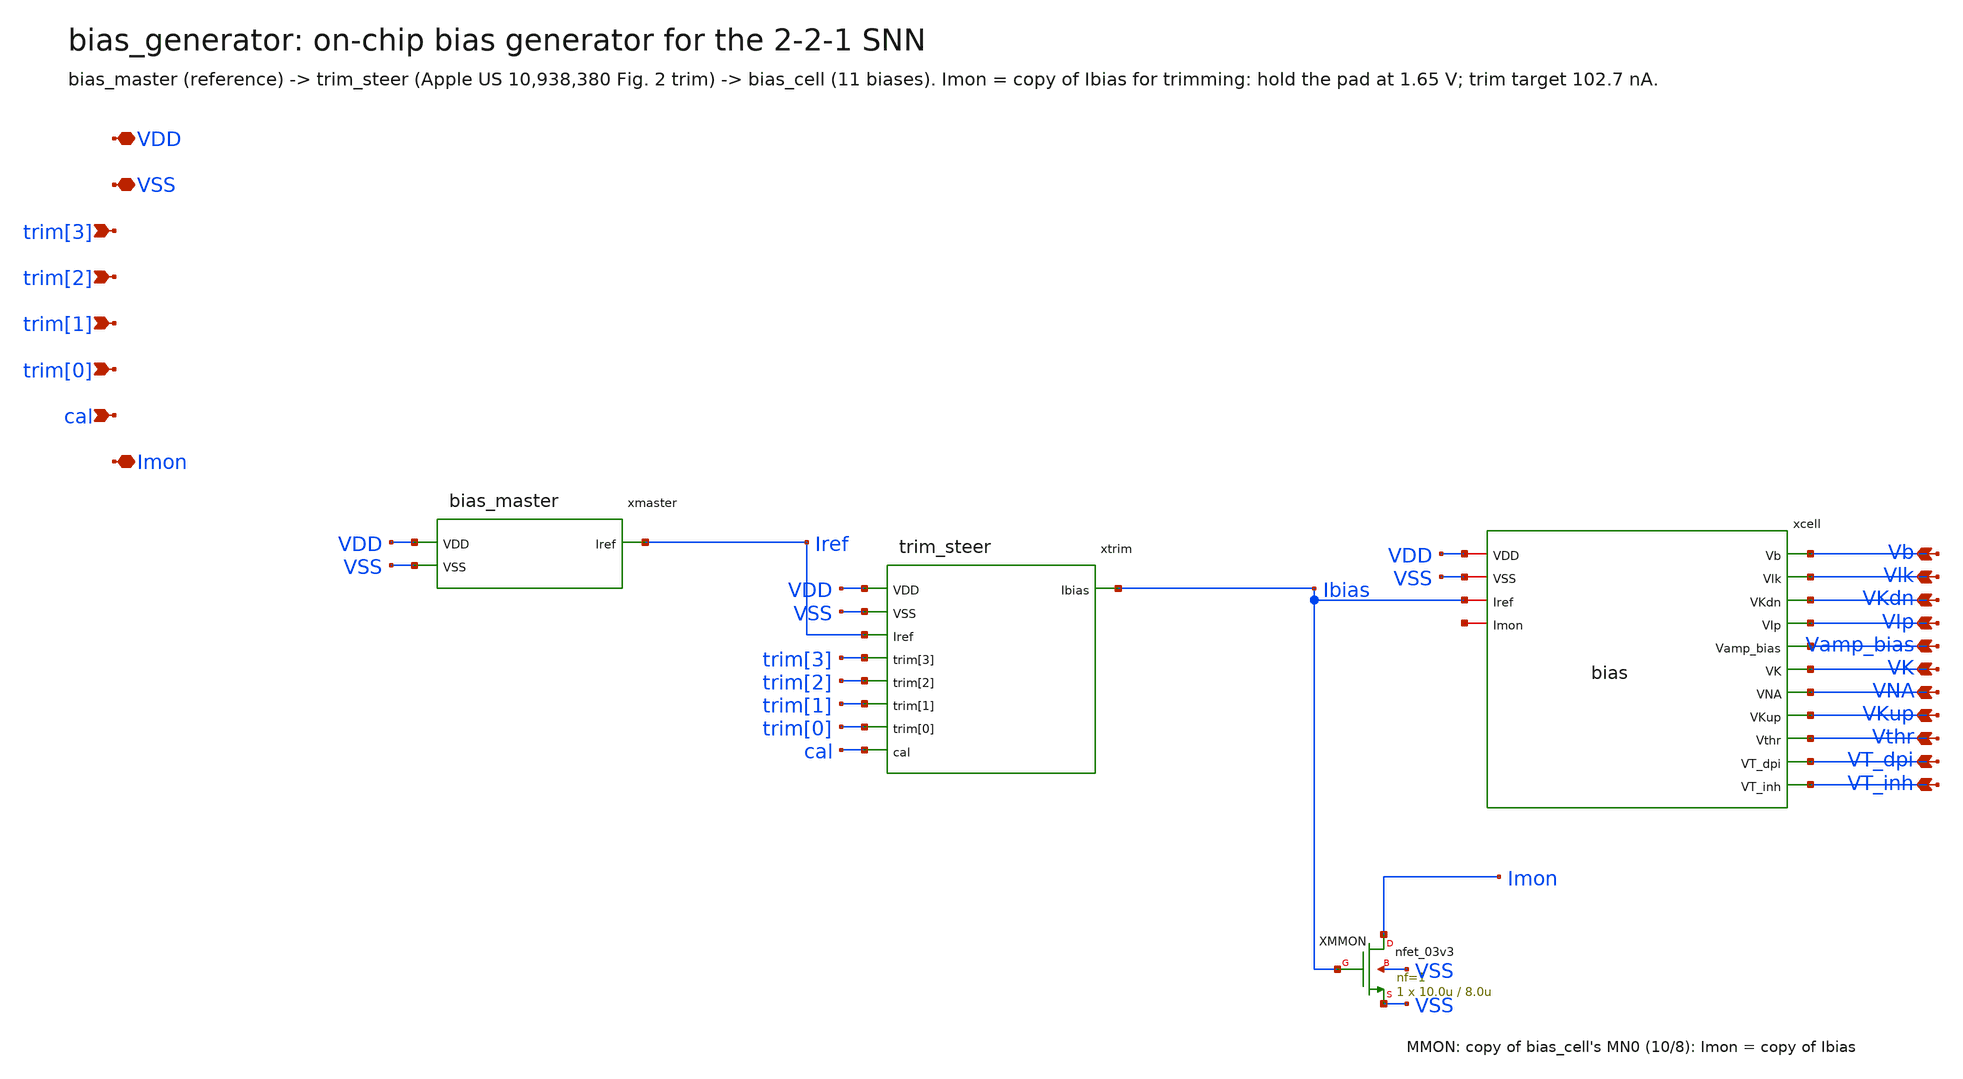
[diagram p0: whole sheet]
** sch_path: explore/bias/generator/bias_generator.sch
**.subckt bias_generator VDD VSS trim[3] trim[2] trim[1] trim[0] cal Imon Vb Vlk VKdn VIp Vamp_bias
*+ VK VNA VKup Vthr VT_dpi VT_inh
*.iopin VDD
*.iopin VSS
*.ipin trim[3]
*.ipin trim[2]
*.ipin trim[1]
*.ipin trim[0]
*.ipin cal
*.iopin Imon
*.opin Vb
*.opin Vlk
*.opin VKdn
*.opin VIp
*.opin Vamp_bias
*.opin VK
*.opin VNA
*.opin VKup
*.opin Vthr
*.opin VT_dpi
*.opin VT_inh
xmaster VDD VSS Iref bias_master
xtrim VDD VSS Iref Ibias trim[3] trim[2] trim[1] trim[0] cal trim_steer
xcell VDD VSS Ibias Vb Vlk VKdn VIp Vamp_bias VK VNA VKup Vthr VT_dpi VT_inh net1 bias
XMMON Imon Ibias VSS VSS nfet_03v3 L=8.0u W=10.0u nf=1 ad='int((nf+1)/2) * W/nf * 0.18u' as='int((nf+2)/2) * W/nf * 0.18u'
+ pd='2*int((nf+1)/2) * (W/nf + 0.18u)' ps='2*int((nf+2)/2) * (W/nf + 0.18u)' nrd='0.18u / W' nrs='0.18u / W'
+ sa=0 sb=0 sd=0 m=1
**.ends

* expanding   symbol:  explore/bias/generator/bias_master.sym # of pins=3
** sym_path: analog/bias/generator/bias_master.sym
** sch_path: analog/bias/generator/bias_master.sch
.subckt bias_master VDD VSS Iref
*.iopin VDD
*.iopin VSS
*.iopin Iref
XM3 Vgp Vgp VDD VDD pfet_03v3 L=6.0u W=1.0u nf=1 ad='int((nf+1)/2) * W/nf * 0.18u' as='int((nf+2)/2) * W/nf * 0.18u'
+ pd='2*int((nf+1)/2) * (W/nf + 0.18u)' ps='2*int((nf+2)/2) * (W/nf + 0.18u)' nrd='0.18u / W' nrs='0.18u / W'
+ sa=0 sb=0 sd=0 m=4
XM4 Vgn Vgp VDD VDD pfet_03v3 L=6.0u W=1.0u nf=1 ad='int((nf+1)/2) * W/nf * 0.18u' as='int((nf+2)/2) * W/nf * 0.18u'
+ pd='2*int((nf+1)/2) * (W/nf + 0.18u)' ps='2*int((nf+2)/2) * (W/nf + 0.18u)' nrd='0.18u / W' nrs='0.18u / W'
+ sa=0 sb=0 sd=0 m=4
XM2 Vgp Vgn Vr VSS nfet_03v3 L=6.0u W=1.0u nf=1 ad='int((nf+1)/2) * W/nf * 0.18u' as='int((nf+2)/2) * W/nf * 0.18u'
+ pd='2*int((nf+1)/2) * (W/nf + 0.18u)' ps='2*int((nf+2)/2) * (W/nf + 0.18u)' nrd='0.18u / W' nrs='0.18u / W'
+ sa=0 sb=0 sd=0 m=64
XM1 Vgn Vgn VSS VSS nfet_03v3 L=6.0u W=1.0u nf=1 ad='int((nf+1)/2) * W/nf * 0.18u' as='int((nf+2)/2) * W/nf * 0.18u'
+ pd='2*int((nf+1)/2) * (W/nf + 0.18u)' ps='2*int((nf+2)/2) * (W/nf + 0.18u)' nrd='0.18u / W' nrs='0.18u / W'
+ sa=0 sb=0 sd=0 m=8
XR VSS Vr VSS nwell r_width=2.0e-6 r_length=585.380e-6 m=1
XMS1_0 net1 VSS VDD VDD pfet_03v3 L=45.45u W=0.5u nf=1 ad='int((nf+1)/2) * W/nf * 0.18u' as='int((nf+2)/2) * W/nf * 0.18u'
+ pd='2*int((nf+1)/2) * (W/nf + 0.18u)' ps='2*int((nf+2)/2) * (W/nf + 0.18u)' nrd='0.18u / W' nrs='0.18u / W'
+ sa=0 sb=0 sd=0 m=1
XMS1_1 net2 VSS net1 VDD pfet_03v3 L=45.45u W=0.5u nf=1 ad='int((nf+1)/2) * W/nf * 0.18u' as='int((nf+2)/2) * W/nf * 0.18u'
+ pd='2*int((nf+1)/2) * (W/nf + 0.18u)' ps='2*int((nf+2)/2) * (W/nf + 0.18u)' nrd='0.18u / W' nrs='0.18u / W'
+ sa=0 sb=0 sd=0 m=1
XMS1_2 net3 VSS net2 VDD pfet_03v3 L=45.45u W=0.5u nf=1 ad='int((nf+1)/2) * W/nf * 0.18u' as='int((nf+2)/2) * W/nf * 0.18u'
+ pd='2*int((nf+1)/2) * (W/nf + 0.18u)' ps='2*int((nf+2)/2) * (W/nf + 0.18u)' nrd='0.18u / W' nrs='0.18u / W'
+ sa=0 sb=0 sd=0 m=1
XMS1_3 s4 VSS net3 VDD pfet_03v3 L=45.45u W=0.5u nf=1 ad='int((nf+1)/2) * W/nf * 0.18u' as='int((nf+2)/2) * W/nf * 0.18u'
+ pd='2*int((nf+1)/2) * (W/nf + 0.18u)' ps='2*int((nf+2)/2) * (W/nf + 0.18u)' nrd='0.18u / W' nrs='0.18u / W'
+ sa=0 sb=0 sd=0 m=1
XMS2 X Vgn VSS VSS nfet_03v3 L=6.0u W=1.0u nf=1 ad='int((nf+1)/2) * W/nf * 0.18u' as='int((nf+2)/2) * W/nf * 0.18u'
+ pd='2*int((nf+1)/2) * (W/nf + 0.18u)' ps='2*int((nf+2)/2) * (W/nf + 0.18u)' nrd='0.18u / W' nrs='0.18u / W'
+ sa=0 sb=0 sd=0 m=16
XMS3 Vgp X VSS VSS nfet_03v3 L=4u W=0.5u nf=1 ad='int((nf+1)/2) * W/nf * 0.18u' as='int((nf+2)/2) * W/nf * 0.18u'
+ pd='2*int((nf+1)/2) * (W/nf + 0.18u)' ps='2*int((nf+2)/2) * (W/nf + 0.18u)' nrd='0.18u / W' nrs='0.18u / W'
+ sa=0 sb=0 sd=0 m=1
XMREF Iref Vgn VSS VSS nfet_03v3 L=6.0u W=1.0u nf=1 ad='int((nf+1)/2) * W/nf * 0.18u' as='int((nf+2)/2) * W/nf * 0.18u'
+ pd='2*int((nf+1)/2) * (W/nf + 0.18u)' ps='2*int((nf+2)/2) * (W/nf + 0.18u)' nrd='0.18u / W' nrs='0.18u / W'
+ sa=0 sb=0 sd=0 m=4
XMS1_4 net4 VSS s4 VDD pfet_03v3 L=45.45u W=0.5u nf=1 ad='int((nf+1)/2) * W/nf * 0.18u' as='int((nf+2)/2) * W/nf * 0.18u'
+ pd='2*int((nf+1)/2) * (W/nf + 0.18u)' ps='2*int((nf+2)/2) * (W/nf + 0.18u)' nrd='0.18u / W' nrs='0.18u / W'
+ sa=0 sb=0 sd=0 m=1
XMS1_5 net5 VSS net4 VDD pfet_03v3 L=45.45u W=0.5u nf=1 ad='int((nf+1)/2) * W/nf * 0.18u' as='int((nf+2)/2) * W/nf * 0.18u'
+ pd='2*int((nf+1)/2) * (W/nf + 0.18u)' ps='2*int((nf+2)/2) * (W/nf + 0.18u)' nrd='0.18u / W' nrs='0.18u / W'
+ sa=0 sb=0 sd=0 m=1
XMS1_6 net6 VSS net5 VDD pfet_03v3 L=45.45u W=0.5u nf=1 ad='int((nf+1)/2) * W/nf * 0.18u' as='int((nf+2)/2) * W/nf * 0.18u'
+ pd='2*int((nf+1)/2) * (W/nf + 0.18u)' ps='2*int((nf+2)/2) * (W/nf + 0.18u)' nrd='0.18u / W' nrs='0.18u / W'
+ sa=0 sb=0 sd=0 m=1
XMS1_7 net7 VSS net6 VDD pfet_03v3 L=45.45u W=0.5u nf=1 ad='int((nf+1)/2) * W/nf * 0.18u' as='int((nf+2)/2) * W/nf * 0.18u'
+ pd='2*int((nf+1)/2) * (W/nf + 0.18u)' ps='2*int((nf+2)/2) * (W/nf + 0.18u)' nrd='0.18u / W' nrs='0.18u / W'
+ sa=0 sb=0 sd=0 m=1
XMS1_8 net8 VSS net7 VDD pfet_03v3 L=45.45u W=0.5u nf=1 ad='int((nf+1)/2) * W/nf * 0.18u' as='int((nf+2)/2) * W/nf * 0.18u'
+ pd='2*int((nf+1)/2) * (W/nf + 0.18u)' ps='2*int((nf+2)/2) * (W/nf + 0.18u)' nrd='0.18u / W' nrs='0.18u / W'
+ sa=0 sb=0 sd=0 m=1
XMS1_9 X VSS net8 VDD pfet_03v3 L=45.45u W=0.5u nf=1 ad='int((nf+1)/2) * W/nf * 0.18u' as='int((nf+2)/2) * W/nf * 0.18u'
+ pd='2*int((nf+1)/2) * (W/nf + 0.18u)' ps='2*int((nf+2)/2) * (W/nf + 0.18u)' nrd='0.18u / W' nrs='0.18u / W'
+ sa=0 sb=0 sd=0 m=1
.ends


* expanding   symbol:  explore/bias/generator/trim_steer.sym # of pins=9
** sym_path: analog/bias/generator/trim_steer.sym
** sch_path: analog/bias/generator/trim_steer.sch
.subckt trim_steer VDD VSS Iref Ibias trim[3] trim[2] trim[1] trim[0] cal
*.iopin VDD
*.iopin VSS
*.iopin Iref
*.ipin trim[3]
*.ipin trim[2]
*.ipin trim[1]
*.ipin trim[0]
*.ipin cal
*.opin Ibias
XM0 Iref Iref VDD VDD pfet_03v3 L=6.0u W=1.0u nf=1 ad='int((nf+1)/2) * W/nf * 0.18u' as='int((nf+2)/2) * W/nf * 0.18u'
+ pd='2*int((nf+1)/2) * (W/nf + 0.18u)' ps='2*int((nf+2)/2) * (W/nf + 0.18u)' nrd='0.18u / W' nrs='0.18u / W'
+ sa=0 sb=0 sd=0 m=23
XR0 Iref Vgs VSS nwell r_width=2.0e-6 r_length=150.000e-6 m=1
XMCG VDD Vgs VDD VDD pfet_03v3 L=10.0u W=10.0u nf=1 ad='int((nf+1)/2) * W/nf * 0.18u' as='int((nf+2)/2) * W/nf * 0.18u'
+ pd='2*int((nf+1)/2) * (W/nf + 0.18u)' ps='2*int((nf+2)/2) * (W/nf + 0.18u)' nrd='0.18u / W' nrs='0.18u / W'
+ sa=0 sb=0 sd=0 m=1
XMB net1 Vgs VDD VDD pfet_03v3 L=6.0u W=1.0u nf=1 ad='int((nf+1)/2) * W/nf * 0.18u' as='int((nf+2)/2) * W/nf * 0.18u'
+ pd='2*int((nf+1)/2) * (W/nf + 0.18u)' ps='2*int((nf+2)/2) * (W/nf + 0.18u)' nrd='0.18u / W' nrs='0.18u / W'
+ sa=0 sb=0 sd=0 m=14
XSB net1 VDD Ibias VSS nfet_03v3 L=0.5u W=1.0u nf=1 ad='int((nf+1)/2) * W/nf * 0.18u' as='int((nf+2)/2) * W/nf * 0.18u'
+ pd='2*int((nf+1)/2) * (W/nf + 0.18u)' ps='2*int((nf+2)/2) * (W/nf + 0.18u)' nrd='0.18u / W' nrs='0.18u / W'
+ sa=0 sb=0 sd=0 m=1
XM1 net2 Vgs VDD VDD pfet_03v3 L=6.0u W=1.0u nf=1 ad='int((nf+1)/2) * W/nf * 0.18u' as='int((nf+2)/2) * W/nf * 0.18u'
+ pd='2*int((nf+1)/2) * (W/nf + 0.18u)' ps='2*int((nf+2)/2) * (W/nf + 0.18u)' nrd='0.18u / W' nrs='0.18u / W'
+ sa=0 sb=0 sd=0 m=1
XS0 net2 trim[0] Ibias VSS nfet_03v3 L=0.5u W=1.0u nf=1 ad='int((nf+1)/2) * W/nf * 0.18u' as='int((nf+2)/2) * W/nf * 0.18u'
+ pd='2*int((nf+1)/2) * (W/nf + 0.18u)' ps='2*int((nf+2)/2) * (W/nf + 0.18u)' nrd='0.18u / W' nrs='0.18u / W'
+ sa=0 sb=0 sd=0 m=1
XS0X net2 tb0 aux VSS nfet_03v3 L=0.5u W=1.0u nf=1 ad='int((nf+1)/2) * W/nf * 0.18u' as='int((nf+2)/2) * W/nf * 0.18u'
+ pd='2*int((nf+1)/2) * (W/nf + 0.18u)' ps='2*int((nf+2)/2) * (W/nf + 0.18u)' nrd='0.18u / W' nrs='0.18u / W'
+ sa=0 sb=0 sd=0 m=1
XM2 net3 Vgs VDD VDD pfet_03v3 L=6.0u W=1.0u nf=1 ad='int((nf+1)/2) * W/nf * 0.18u' as='int((nf+2)/2) * W/nf * 0.18u'
+ pd='2*int((nf+1)/2) * (W/nf + 0.18u)' ps='2*int((nf+2)/2) * (W/nf + 0.18u)' nrd='0.18u / W' nrs='0.18u / W'
+ sa=0 sb=0 sd=0 m=2
XS1 net3 trim[1] Ibias VSS nfet_03v3 L=0.5u W=1.0u nf=1 ad='int((nf+1)/2) * W/nf * 0.18u' as='int((nf+2)/2) * W/nf * 0.18u'
+ pd='2*int((nf+1)/2) * (W/nf + 0.18u)' ps='2*int((nf+2)/2) * (W/nf + 0.18u)' nrd='0.18u / W' nrs='0.18u / W'
+ sa=0 sb=0 sd=0 m=1
XS1X net3 tb1 aux VSS nfet_03v3 L=0.5u W=1.0u nf=1 ad='int((nf+1)/2) * W/nf * 0.18u' as='int((nf+2)/2) * W/nf * 0.18u'
+ pd='2*int((nf+1)/2) * (W/nf + 0.18u)' ps='2*int((nf+2)/2) * (W/nf + 0.18u)' nrd='0.18u / W' nrs='0.18u / W'
+ sa=0 sb=0 sd=0 m=1
XM3 net4 Vgs VDD VDD pfet_03v3 L=6.0u W=1.0u nf=1 ad='int((nf+1)/2) * W/nf * 0.18u' as='int((nf+2)/2) * W/nf * 0.18u'
+ pd='2*int((nf+1)/2) * (W/nf + 0.18u)' ps='2*int((nf+2)/2) * (W/nf + 0.18u)' nrd='0.18u / W' nrs='0.18u / W'
+ sa=0 sb=0 sd=0 m=4
XS2 net4 trim[2] Ibias VSS nfet_03v3 L=0.5u W=1.0u nf=1 ad='int((nf+1)/2) * W/nf * 0.18u' as='int((nf+2)/2) * W/nf * 0.18u'
+ pd='2*int((nf+1)/2) * (W/nf + 0.18u)' ps='2*int((nf+2)/2) * (W/nf + 0.18u)' nrd='0.18u / W' nrs='0.18u / W'
+ sa=0 sb=0 sd=0 m=1
XS2X net4 tb2 aux VSS nfet_03v3 L=0.5u W=1.0u nf=1 ad='int((nf+1)/2) * W/nf * 0.18u' as='int((nf+2)/2) * W/nf * 0.18u'
+ pd='2*int((nf+1)/2) * (W/nf + 0.18u)' ps='2*int((nf+2)/2) * (W/nf + 0.18u)' nrd='0.18u / W' nrs='0.18u / W'
+ sa=0 sb=0 sd=0 m=1
XM4 net5 Vgs VDD VDD pfet_03v3 L=6.0u W=1.0u nf=1 ad='int((nf+1)/2) * W/nf * 0.18u' as='int((nf+2)/2) * W/nf * 0.18u'
+ pd='2*int((nf+1)/2) * (W/nf + 0.18u)' ps='2*int((nf+2)/2) * (W/nf + 0.18u)' nrd='0.18u / W' nrs='0.18u / W'
+ sa=0 sb=0 sd=0 m=8
XS3 net5 trim[3] Ibias VSS nfet_03v3 L=0.5u W=1.0u nf=1 ad='int((nf+1)/2) * W/nf * 0.18u' as='int((nf+2)/2) * W/nf * 0.18u'
+ pd='2*int((nf+1)/2) * (W/nf + 0.18u)' ps='2*int((nf+2)/2) * (W/nf + 0.18u)' nrd='0.18u / W' nrs='0.18u / W'
+ sa=0 sb=0 sd=0 m=1
XS3X net5 tb3 aux VSS nfet_03v3 L=0.5u W=1.0u nf=1 ad='int((nf+1)/2) * W/nf * 0.18u' as='int((nf+2)/2) * W/nf * 0.18u'
+ pd='2*int((nf+1)/2) * (W/nf + 0.18u)' ps='2*int((nf+2)/2) * (W/nf + 0.18u)' nrd='0.18u / W' nrs='0.18u / W'
+ sa=0 sb=0 sd=0 m=1
XMIP0 tb0 trim[0] VDD VDD pfet_03v3 L=0.28u W=1.0u nf=1 ad='int((nf+1)/2) * W/nf * 0.18u' as='int((nf+2)/2) * W/nf * 0.18u'
+ pd='2*int((nf+1)/2) * (W/nf + 0.18u)' ps='2*int((nf+2)/2) * (W/nf + 0.18u)' nrd='0.18u / W' nrs='0.18u / W'
+ sa=0 sb=0 sd=0 m=1
XMIN0 tb0 trim[0] VSS VSS nfet_03v3 L=0.28u W=0.5u nf=1 ad='int((nf+1)/2) * W/nf * 0.18u' as='int((nf+2)/2) * W/nf * 0.18u'
+ pd='2*int((nf+1)/2) * (W/nf + 0.18u)' ps='2*int((nf+2)/2) * (W/nf + 0.18u)' nrd='0.18u / W' nrs='0.18u / W'
+ sa=0 sb=0 sd=0 m=1
XMIP1 tb1 trim[1] VDD VDD pfet_03v3 L=0.28u W=1.0u nf=1 ad='int((nf+1)/2) * W/nf * 0.18u' as='int((nf+2)/2) * W/nf * 0.18u'
+ pd='2*int((nf+1)/2) * (W/nf + 0.18u)' ps='2*int((nf+2)/2) * (W/nf + 0.18u)' nrd='0.18u / W' nrs='0.18u / W'
+ sa=0 sb=0 sd=0 m=1
XMIN1 tb1 trim[1] VSS VSS nfet_03v3 L=0.28u W=0.5u nf=1 ad='int((nf+1)/2) * W/nf * 0.18u' as='int((nf+2)/2) * W/nf * 0.18u'
+ pd='2*int((nf+1)/2) * (W/nf + 0.18u)' ps='2*int((nf+2)/2) * (W/nf + 0.18u)' nrd='0.18u / W' nrs='0.18u / W'
+ sa=0 sb=0 sd=0 m=1
XMIP2 tb2 trim[2] VDD VDD pfet_03v3 L=0.28u W=1.0u nf=1 ad='int((nf+1)/2) * W/nf * 0.18u' as='int((nf+2)/2) * W/nf * 0.18u'
+ pd='2*int((nf+1)/2) * (W/nf + 0.18u)' ps='2*int((nf+2)/2) * (W/nf + 0.18u)' nrd='0.18u / W' nrs='0.18u / W'
+ sa=0 sb=0 sd=0 m=1
XMIN2 tb2 trim[2] VSS VSS nfet_03v3 L=0.28u W=0.5u nf=1 ad='int((nf+1)/2) * W/nf * 0.18u' as='int((nf+2)/2) * W/nf * 0.18u'
+ pd='2*int((nf+1)/2) * (W/nf + 0.18u)' ps='2*int((nf+2)/2) * (W/nf + 0.18u)' nrd='0.18u / W' nrs='0.18u / W'
+ sa=0 sb=0 sd=0 m=1
XMIP3 tb3 trim[3] VDD VDD pfet_03v3 L=0.28u W=1.0u nf=1 ad='int((nf+1)/2) * W/nf * 0.18u' as='int((nf+2)/2) * W/nf * 0.18u'
+ pd='2*int((nf+1)/2) * (W/nf + 0.18u)' ps='2*int((nf+2)/2) * (W/nf + 0.18u)' nrd='0.18u / W' nrs='0.18u / W'
+ sa=0 sb=0 sd=0 m=1
XMIN3 tb3 trim[3] VSS VSS nfet_03v3 L=0.28u W=0.5u nf=1 ad='int((nf+1)/2) * W/nf * 0.18u' as='int((nf+2)/2) * W/nf * 0.18u'
+ pd='2*int((nf+1)/2) * (W/nf + 0.18u)' ps='2*int((nf+2)/2) * (W/nf + 0.18u)' nrd='0.18u / W' nrs='0.18u / W'
+ sa=0 sb=0 sd=0 m=1
XMAUX aux vaux VSS VSS nfet_03v3 L=8.0u W=10.0u nf=1 ad='int((nf+1)/2) * W/nf * 0.18u' as='int((nf+2)/2) * W/nf * 0.18u'
+ pd='2*int((nf+1)/2) * (W/nf + 0.18u)' ps='2*int((nf+2)/2) * (W/nf + 0.18u)' nrd='0.18u / W' nrs='0.18u / W'
+ sa=0 sb=0 sd=0 m=1
XMCAL aux cal vaux VSS nfet_03v3 L=0.5u W=1.0u nf=1 ad='int((nf+1)/2) * W/nf * 0.18u' as='int((nf+2)/2) * W/nf * 0.18u'
+ pd='2*int((nf+1)/2) * (W/nf + 0.18u)' ps='2*int((nf+2)/2) * (W/nf + 0.18u)' nrd='0.18u / W' nrs='0.18u / W'
+ sa=0 sb=0 sd=0 m=1
XMDIS vaux calb VSS VSS nfet_03v3 L=45.45u W=0.5u nf=1 ad='int((nf+1)/2) * W/nf * 0.18u' as='int((nf+2)/2) * W/nf * 0.18u'
+ pd='2*int((nf+1)/2) * (W/nf + 0.18u)' ps='2*int((nf+2)/2) * (W/nf + 0.18u)' nrd='0.18u / W' nrs='0.18u / W'
+ sa=0 sb=0 sd=0 m=1
XMCAUX VSS vaux VSS VSS nfet_03v3 L=5.0u W=5.0u nf=1 ad='int((nf+1)/2) * W/nf * 0.18u' as='int((nf+2)/2) * W/nf * 0.18u'
+ pd='2*int((nf+1)/2) * (W/nf + 0.18u)' ps='2*int((nf+2)/2) * (W/nf + 0.18u)' nrd='0.18u / W' nrs='0.18u / W'
+ sa=0 sb=0 sd=0 m=1
XMIPC calb cal VDD VDD pfet_03v3 L=0.28u W=1.0u nf=1 ad='int((nf+1)/2) * W/nf * 0.18u' as='int((nf+2)/2) * W/nf * 0.18u'
+ pd='2*int((nf+1)/2) * (W/nf + 0.18u)' ps='2*int((nf+2)/2) * (W/nf + 0.18u)' nrd='0.18u / W' nrs='0.18u / W'
+ sa=0 sb=0 sd=0 m=1
XMINC calb cal VSS VSS nfet_03v3 L=0.28u W=0.5u nf=1 ad='int((nf+1)/2) * W/nf * 0.18u' as='int((nf+2)/2) * W/nf * 0.18u'
+ pd='2*int((nf+1)/2) * (W/nf + 0.18u)' ps='2*int((nf+2)/2) * (W/nf + 0.18u)' nrd='0.18u / W' nrs='0.18u / W'
+ sa=0 sb=0 sd=0 m=1
.ends


* expanding   symbol:  bias.sym # of pins=15
** sym_path: analog/neuron/bias.sym
** sch_path: analog/neuron/bias.sch
.subckt bias VDD VSS Iref Vb Vlk VKdn VIp Vamp_bias VK VNA VKup Vthr VT_dpi VT_inh Imon
*.iopin VDD
*.iopin VSS
*.iopin Iref
*.opin Vb
*.opin Vlk
*.opin VKdn
*.opin VIp
*.opin Vamp_bias
*.opin VK
*.opin VNA
*.opin VKup
*.opin Vthr
*.opin VT_dpi
*.opin VT_inh
*.iopin Imon
XMN0 Iref Iref VSS VSS nfet_03v3 L=8u W=10u nf=1 ad='int((nf+1)/2) * W/nf * 0.18u' as='int((nf+2)/2) * W/nf * 0.18u'
+ pd='2*int((nf+1)/2) * (W/nf + 0.18u)' ps='2*int((nf+2)/2) * (W/nf + 0.18u)' nrd='0.18u / W' nrs='0.18u / W'
+ sa=0 sb=0 sd=0 m=1
XMNP vgp Iref VSS VSS nfet_03v3 L=8u W=10u nf=1 ad='int((nf+1)/2) * W/nf * 0.18u' as='int((nf+2)/2) * W/nf * 0.18u'
+ pd='2*int((nf+1)/2) * (W/nf + 0.18u)' ps='2*int((nf+2)/2) * (W/nf + 0.18u)' nrd='0.18u / W' nrs='0.18u / W'
+ sa=0 sb=0 sd=0 m=1
XMP0 vgp vgp VDD VDD pfet_03v3 L=8u W=10u nf=1 ad='int((nf+1)/2) * W/nf * 0.18u' as='int((nf+2)/2) * W/nf * 0.18u'
+ pd='2*int((nf+1)/2) * (W/nf + 0.18u)' ps='2*int((nf+2)/2) * (W/nf + 0.18u)' nrd='0.18u / W' nrs='0.18u / W'
+ sa=0 sb=0 sd=0 m=1
XMO_Vb Vb vgp VDD VDD pfet_03v3 L=8u W=1.44u nf=1 ad='int((nf+1)/2) * W/nf * 0.18u' as='int((nf+2)/2) * W/nf * 0.18u'
+ pd='2*int((nf+1)/2) * (W/nf + 0.18u)' ps='2*int((nf+2)/2) * (W/nf + 0.18u)' nrd='0.18u / W' nrs='0.18u / W'
+ sa=0 sb=0 sd=0 m=1
XMR_Vb Vb Vb VSS VSS nfet_03v3 L=8u W=1u nf=1 ad='int((nf+1)/2) * W/nf * 0.18u' as='int((nf+2)/2) * W/nf * 0.18u'
+ pd='2*int((nf+1)/2) * (W/nf + 0.18u)' ps='2*int((nf+2)/2) * (W/nf + 0.18u)' nrd='0.18u / W' nrs='0.18u / W'
+ sa=0 sb=0 sd=0 m=1
XMO_Vlk Vlk vgp VDD VDD pfet_03v3 L=16u W=0.84u nf=1 ad='int((nf+1)/2) * W/nf * 0.18u' as='int((nf+2)/2) * W/nf * 0.18u'
+ pd='2*int((nf+1)/2) * (W/nf + 0.18u)' ps='2*int((nf+2)/2) * (W/nf + 0.18u)' nrd='0.18u / W' nrs='0.18u / W'
+ sa=0 sb=0 sd=0 m=1
XMR_Vlk Vlk Vlk VSS VSS nfet_03v3 L=1u W=1u nf=1 ad='int((nf+1)/2) * W/nf * 0.18u' as='int((nf+2)/2) * W/nf * 0.18u'
+ pd='2*int((nf+1)/2) * (W/nf + 0.18u)' ps='2*int((nf+2)/2) * (W/nf + 0.18u)' nrd='0.18u / W' nrs='0.18u / W'
+ sa=0 sb=0 sd=0 m=8
XMO_VKdn VKdn vgp VDD VDD pfet_03v3 L=8u W=12.94u nf=1 ad='int((nf+1)/2) * W/nf * 0.18u' as='int((nf+2)/2) * W/nf * 0.18u'
+ pd='2*int((nf+1)/2) * (W/nf + 0.18u)' ps='2*int((nf+2)/2) * (W/nf + 0.18u)' nrd='0.18u / W' nrs='0.18u / W'
+ sa=0 sb=0 sd=0 m=1
XMR_VKdn VKdn VKdn VSS VSS nfet_03v3 L=1u W=1u nf=1 ad='int((nf+1)/2) * W/nf * 0.18u' as='int((nf+2)/2) * W/nf * 0.18u'
+ pd='2*int((nf+1)/2) * (W/nf + 0.18u)' ps='2*int((nf+2)/2) * (W/nf + 0.18u)' nrd='0.18u / W' nrs='0.18u / W'
+ sa=0 sb=0 sd=0 m=4
XMO_VIp VIp vgp VDD VDD pfet_03v3 L=8u W=2.34u nf=1 ad='int((nf+1)/2) * W/nf * 0.18u' as='int((nf+2)/2) * W/nf * 0.18u'
+ pd='2*int((nf+1)/2) * (W/nf + 0.18u)' ps='2*int((nf+2)/2) * (W/nf + 0.18u)' nrd='0.18u / W' nrs='0.18u / W'
+ sa=0 sb=0 sd=0 m=1
XMR_VIp VIp VIp VSS VSS nfet_03v3 L=1u W=1u nf=1 ad='int((nf+1)/2) * W/nf * 0.18u' as='int((nf+2)/2) * W/nf * 0.18u'
+ pd='2*int((nf+1)/2) * (W/nf + 0.18u)' ps='2*int((nf+2)/2) * (W/nf + 0.18u)' nrd='0.18u / W' nrs='0.18u / W'
+ sa=0 sb=0 sd=0 m=1
XMO_Vamp_bias Vamp_bias vgp VDD VDD pfet_03v3 L=8u W=9.14u nf=1 ad='int((nf+1)/2) * W/nf * 0.18u' as='int((nf+2)/2) * W/nf * 0.18u'
+ pd='2*int((nf+1)/2) * (W/nf + 0.18u)' ps='2*int((nf+2)/2) * (W/nf + 0.18u)' nrd='0.18u / W' nrs='0.18u / W'
+ sa=0 sb=0 sd=0 m=1
XMR_Vamp_bias Vamp_bias Vamp_bias VSS VSS nfet_03v3 L=0.64u W=0.5u nf=1 ad='int((nf+1)/2) * W/nf * 0.18u'
+ as='int((nf+2)/2) * W/nf * 0.18u' pd='2*int((nf+1)/2) * (W/nf + 0.18u)' ps='2*int((nf+2)/2) * (W/nf + 0.18u)'
+ nrd='0.18u / W' nrs='0.18u / W' sa=0 sb=0 sd=0 m=1
XMO_VK VK vgp VDD VDD pfet_03v3 L=8u W=10.45u nf=1 ad='int((nf+1)/2) * W/nf * 0.18u' as='int((nf+2)/2) * W/nf * 0.18u'
+ pd='2*int((nf+1)/2) * (W/nf + 0.18u)' ps='2*int((nf+2)/2) * (W/nf + 0.18u)' nrd='0.18u / W' nrs='0.18u / W'
+ sa=0 sb=0 sd=0 m=1
XMR_VK VK VK vk_mid VSS nfet_03v3 L=45.45u W=0.5u nf=1 ad='int((nf+1)/2) * W/nf * 0.18u' as='int((nf+2)/2) * W/nf * 0.18u'
+ pd='2*int((nf+1)/2) * (W/nf + 0.18u)' ps='2*int((nf+2)/2) * (W/nf + 0.18u)' nrd='0.18u / W' nrs='0.18u / W'
+ sa=0 sb=0 sd=0 m=1
XMR_VNA VNA VNA VDD VDD pfet_03v3 L=45.45u W=0.5u nf=1 ad='int((nf+1)/2) * W/nf * 0.18u' as='int((nf+2)/2) * W/nf * 0.18u'
+ pd='2*int((nf+1)/2) * (W/nf + 0.18u)' ps='2*int((nf+2)/2) * (W/nf + 0.18u)' nrd='0.18u / W' nrs='0.18u / W'
+ sa=0 sb=0 sd=0 m=1
XMO_VNA VNA Iref VSS VSS nfet_03v3 L=8u W=5.76u nf=1 ad='int((nf+1)/2) * W/nf * 0.18u' as='int((nf+2)/2) * W/nf * 0.18u'
+ pd='2*int((nf+1)/2) * (W/nf + 0.18u)' ps='2*int((nf+2)/2) * (W/nf + 0.18u)' nrd='0.18u / W' nrs='0.18u / W'
+ sa=0 sb=0 sd=0 m=1
XMR_VKup VKup VKup VDD VDD pfet_03v3 L=8u W=1u nf=1 ad='int((nf+1)/2) * W/nf * 0.18u' as='int((nf+2)/2) * W/nf * 0.18u'
+ pd='2*int((nf+1)/2) * (W/nf + 0.18u)' ps='2*int((nf+2)/2) * (W/nf + 0.18u)' nrd='0.18u / W' nrs='0.18u / W'
+ sa=0 sb=0 sd=0 m=1
XMO_VKup VKup Iref VSS VSS nfet_03v3 L=8u W=6.01u nf=1 ad='int((nf+1)/2) * W/nf * 0.18u' as='int((nf+2)/2) * W/nf * 0.18u'
+ pd='2*int((nf+1)/2) * (W/nf + 0.18u)' ps='2*int((nf+2)/2) * (W/nf + 0.18u)' nrd='0.18u / W' nrs='0.18u / W'
+ sa=0 sb=0 sd=0 m=1
XMR_Vthr Vthr Vthr VDD VDD pfet_03v3 L=5.12u W=4u nf=1 ad='int((nf+1)/2) * W/nf * 0.18u' as='int((nf+2)/2) * W/nf * 0.18u'
+ pd='2*int((nf+1)/2) * (W/nf + 0.18u)' ps='2*int((nf+2)/2) * (W/nf + 0.18u)' nrd='0.18u / W' nrs='0.18u / W'
+ sa=0 sb=0 sd=0 m=32
XMO_Vthr Vthr Iref VSS VSS nfet_03v3 L=32u W=0.91u nf=1 ad='int((nf+1)/2) * W/nf * 0.18u' as='int((nf+2)/2) * W/nf * 0.18u'
+ pd='2*int((nf+1)/2) * (W/nf + 0.18u)' ps='2*int((nf+2)/2) * (W/nf + 0.18u)' nrd='0.18u / W' nrs='0.18u / W'
+ sa=0 sb=0 sd=0 m=1
XMR_VT_dpi VT_dpi VT_dpi VDD VDD pfet_03v3 L=5.12u W=4u nf=1 ad='int((nf+1)/2) * W/nf * 0.18u' as='int((nf+2)/2) * W/nf * 0.18u'
+ pd='2*int((nf+1)/2) * (W/nf + 0.18u)' ps='2*int((nf+2)/2) * (W/nf + 0.18u)' nrd='0.18u / W' nrs='0.18u / W'
+ sa=0 sb=0 sd=0 m=32
XMO_VT_dpi VT_dpi Iref VSS VSS nfet_03v3 L=32u W=1.17u nf=1 ad='int((nf+1)/2) * W/nf * 0.18u' as='int((nf+2)/2) * W/nf * 0.18u'
+ pd='2*int((nf+1)/2) * (W/nf + 0.18u)' ps='2*int((nf+2)/2) * (W/nf + 0.18u)' nrd='0.18u / W' nrs='0.18u / W'
+ sa=0 sb=0 sd=0 m=1
XMR_VT_inh VT_inh VT_inh VDD VDD pfet_03v3 L=1.12u W=0.88u nf=1 ad='int((nf+1)/2) * W/nf * 0.18u' as='int((nf+2)/2) * W/nf * 0.18u'
+ pd='2*int((nf+1)/2) * (W/nf + 0.18u)' ps='2*int((nf+2)/2) * (W/nf + 0.18u)' nrd='0.18u / W' nrs='0.18u / W'
+ sa=0 sb=0 sd=0 m=16
XMO_VT_inh VT_inh Iref VSS VSS nfet_03v3 L=32u W=0.63u nf=1 ad='int((nf+1)/2) * W/nf * 0.18u' as='int((nf+2)/2) * W/nf * 0.18u'
+ pd='2*int((nf+1)/2) * (W/nf + 0.18u)' ps='2*int((nf+2)/2) * (W/nf + 0.18u)' nrd='0.18u / W' nrs='0.18u / W'
+ sa=0 sb=0 sd=0 m=1
XMR_VK2 vk_mid VK VSS VSS nfet_03v3 L=45.45u W=0.5u nf=1 ad='int((nf+1)/2) * W/nf * 0.18u' as='int((nf+2)/2) * W/nf * 0.18u'
+ pd='2*int((nf+1)/2) * (W/nf + 0.18u)' ps='2*int((nf+2)/2) * (W/nf + 0.18u)' nrd='0.18u / W' nrs='0.18u / W'
+ sa=0 sb=0 sd=0 m=1
XMMON Imon Iref VSS VSS nfet_03v3 L=8u W=10u nf=1 ad='int((nf+1)/2) * W/nf * 0.18u' as='int((nf+2)/2) * W/nf * 0.18u'
+ pd='2*int((nf+1)/2) * (W/nf + 0.18u)' ps='2*int((nf+2)/2) * (W/nf + 0.18u)' nrd='0.18u / W' nrs='0.18u / W'
+ sa=0 sb=0 sd=0 m=1
.ends

.end
